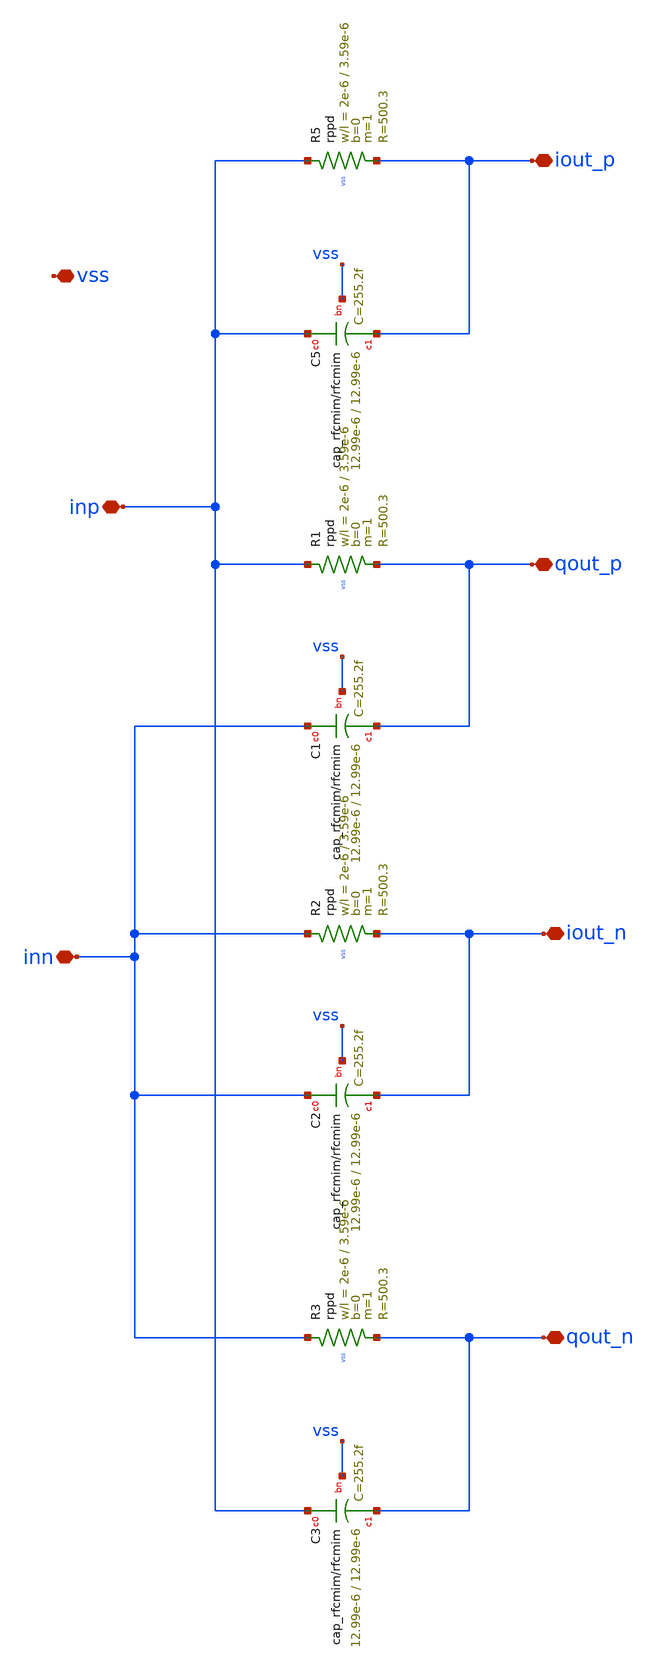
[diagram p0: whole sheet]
** sch_path: LNA7096-main/schematic/xschem/04_iq_ppf/ppf01.sch
**.subckt ppf01 inp inn iout_p qout_p iout_n qout_n vss
*.iopin inp
*.iopin inn
*.iopin iout_p
*.iopin qout_p
*.iopin iout_n
*.iopin qout_n
*.iopin vss
XR5 inp iout_p vss rppd w=2e-6 l=3.59e-6 m=1 b=0 mm_ok=1
XR1 inp qout_p vss rppd w=2e-6 l=3.59e-6 m=1 b=0 mm_ok=1
XR2 inn iout_n vss rppd w=2e-6 l=3.59e-6 m=1 b=0 mm_ok=1
XR3 inn qout_n vss rppd w=2e-6 l=3.59e-6 m=1 b=0 mm_ok=1
XC5 inp iout_p vss cap_rfcmim w=12.99e-6 l=12.99e-6 wfeed=3.0e-6 m=1 mm_ok=1
XC1 inn qout_p vss cap_rfcmim w=12.99e-6 l=12.99e-6 wfeed=3.0e-6 m=1 mm_ok=1
XC2 inn iout_n vss cap_rfcmim w=12.99e-6 l=12.99e-6 wfeed=3.0e-6 m=1 mm_ok=1
XC3 inp qout_n vss cap_rfcmim w=12.99e-6 l=12.99e-6 wfeed=3.0e-6 m=1 mm_ok=1
**.ends
.end
